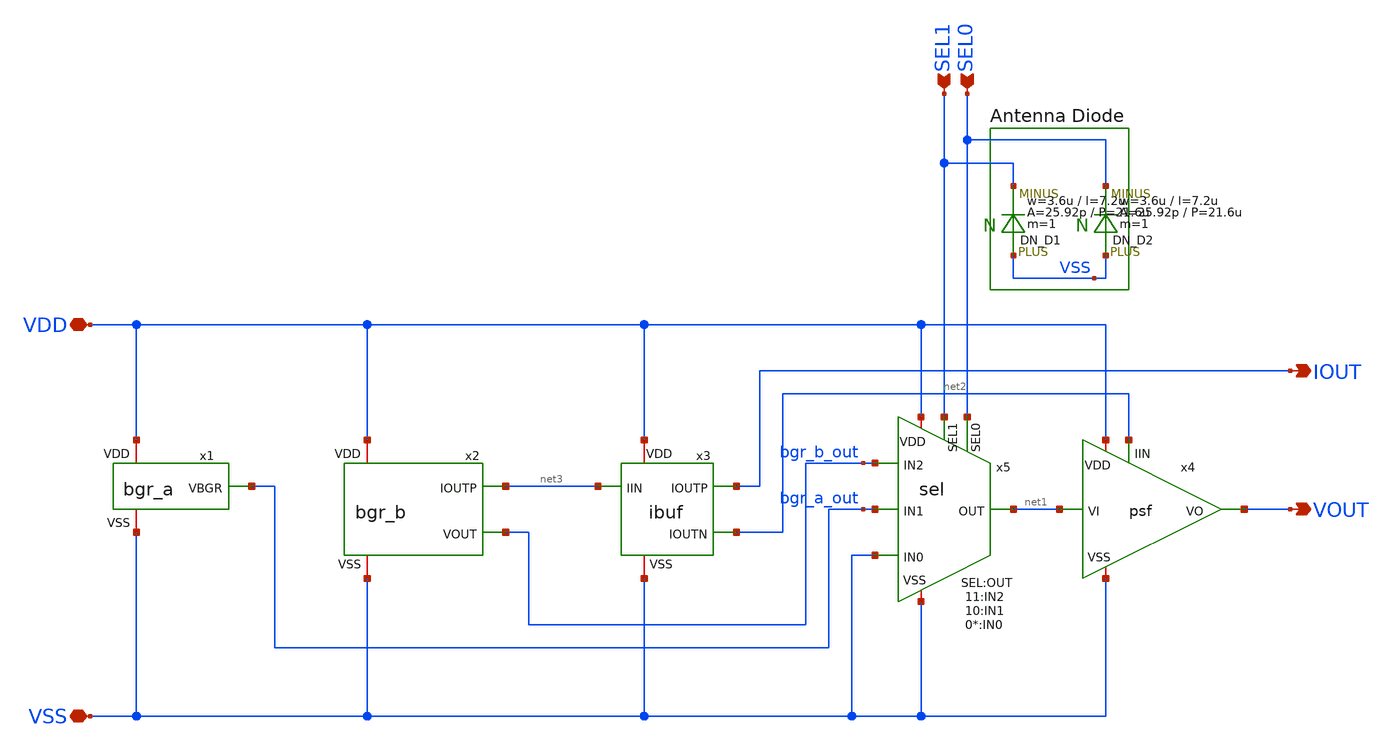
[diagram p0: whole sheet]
** sch_path: member_project/BGR/Maehashi/design/bgr_top.sch
**.subckt bgr_top VOUT IOUT VSS VDD SEL1 SEL0
*.opin VOUT
*.opin IOUT
*.iopin VSS
*.iopin VDD
*.ipin SEL1
*.ipin SEL0
x1 VDD bgr_a_out VSS bgr_a
x2 VDD net3 bgr_b_out VSS bgr_b
x3 VDD IOUT net3 net2 VSS ibuf
x4 VDD net1 VOUT net2 VSS psf
x5 VDD SEL1 net1 bgr_b_out bgr_a_out VSS VSS SEL0 sel
DD1 VSS SEL1 DN m=1
DD2 VSS SEL0 DN m=1
**.ends
.end
